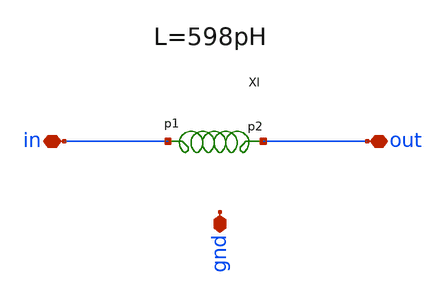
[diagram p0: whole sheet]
** sch_path: impedance-transformer/xschem/impedance-transformer-pex.sch
**.subckt impedance-transformer-pex gnd in out
*.iopin gnd
*.iopin in
*.iopin out
xl1 in out l1
**** begin user architecture code

* NGSPICE file created from impedance-transformer.ext - technology: sky130A

.subckt sky130_fd_pr__cap_mim_m3_2_4GE4YE c2_n2372_n7179# m4_n2472_n7279# VSUBS
X0 c2_n2372_n7179# m4_n2472_n7279# sky130_fd_pr__cap_mim_m3_2 l=2.293e+07u w=2.293e+07u
X1 c2_n2372_n7179# m4_n2472_n7279# sky130_fd_pr__cap_mim_m3_2 l=2.293e+07u w=2.293e+07u
X2 c2_n2372_n7179# m4_n2472_n7279# sky130_fd_pr__cap_mim_m3_2 l=2.293e+07u w=2.293e+07u
C0 m4_n2472_n7279# c2_n2372_n7179# 105.86fF
C1 c2_n2372_n7179# VSUBS 0.26fF
C2 m4_n2472_n7279# VSUBS 28.10fF
.ends

.subckt sky130_fd_pr__cap_mim_m3_2_8BWDGQ c2_n2486_n10078# m4_n2586_n10178# VSUBS
X0 c2_n2486_n10078# m4_n2586_n10178# sky130_fd_pr__cap_mim_m3_2 l=2.407e+07u w=2.407e+07u
X1 c2_n2486_n10078# m4_n2586_n10178# sky130_fd_pr__cap_mim_m3_2 l=2.407e+07u w=2.407e+07u
X2 c2_n2486_n10078# m4_n2586_n10178# sky130_fd_pr__cap_mim_m3_2 l=2.407e+07u w=2.407e+07u
X3 c2_n2486_n10078# m4_n2586_n10178# sky130_fd_pr__cap_mim_m3_2 l=2.407e+07u w=2.407e+07u
C0 m4_n2586_n10178# c2_n2486_n10078# 154.16fF
C1 c2_n2486_n10078# VSUBS 0.30fF
C2 m4_n2586_n10178# VSUBS 40.10fF
.ends

*.subckt impedance-transformer gnd out in
Xsky130_fd_pr__cap_mim_m3_2_4GE4YE_1 in gnd gnd sky130_fd_pr__cap_mim_m3_2_4GE4YE
Xsky130_fd_pr__cap_mim_m3_2_4GE4YE_2 in gnd gnd sky130_fd_pr__cap_mim_m3_2_4GE4YE
Xsky130_fd_pr__cap_mim_m3_2_8BWDGQ_0 out gnd gnd sky130_fd_pr__cap_mim_m3_2_8BWDGQ
Xsky130_fd_pr__cap_mim_m3_2_8BWDGQ_1 out gnd gnd sky130_fd_pr__cap_mim_m3_2_8BWDGQ
Xsky130_fd_pr__cap_mim_m3_2_8BWDGQ_2 out gnd gnd sky130_fd_pr__cap_mim_m3_2_8BWDGQ
Xsky130_fd_pr__cap_mim_m3_2_8BWDGQ_3 out gnd gnd sky130_fd_pr__cap_mim_m3_2_8BWDGQ
Xsky130_fd_pr__cap_mim_m3_2_4GE4YE_0 in gnd gnd sky130_fd_pr__cap_mim_m3_2_4GE4YE

R0 in in.n1 0.704
R1 in.n0 in.t3 0.125
R2 in.n1 in.n0 0.089
R3 in.t8 in.t7 0.066
R4 in.t6 in.t8 0.066
R5 in.t2 in.t1 0.066
R6 in.t0 in.t2 0.066
R7 in.t5 in.t4 0.066
R8 in.t3 in.t5 0.066
R9 in.n1 in.t6 0.037
R10 in.n0 in.t0 0.037
R11 out out.n2 0.325
R12 out.n0 out.t13 0.094
R13 out.n1 out.n0 0.079
R14 out.t14 out.t15 0.066
R15 out.t12 out.t14 0.066
R16 out.t13 out.t12 0.066
R17 out.t10 out.t11 0.066
R18 out.t8 out.t10 0.066
R19 out.t9 out.t8 0.066
R20 out.t6 out.t7 0.066
R21 out.t4 out.t6 0.066
R22 out.t5 out.t4 0.066
R23 out.t2 out.t3 0.066
R24 out.t0 out.t2 0.066
R25 out.t1 out.t0 0.066
R26 out.n2 out.n1 0.064
R27 out.n2 out.t1 0.041
R28 out.n0 out.t9 0.018
R29 out.n1 out.t5 0.018
C0 out.t7 gnd 33.56fF
C1 out.t6 gnd 33.64fF
C2 out.t4 gnd 33.64fF
C3 out.t5 gnd 29.89fF
C4 out.t11 gnd 33.56fF
C5 out.t10 gnd 33.64fF
C6 out.t8 gnd 33.64fF
C7 out.t9 gnd 29.89fF
C8 out.t15 gnd 33.56fF
C9 out.t14 gnd 33.64fF
C10 out.t12 gnd 33.64fF
C11 out.t13 gnd 89.97fF
C12 out.n0 gnd 28.18fF $ **FLOATING
C13 out.n1 gnd 13.26fF $ **FLOATING
C14 out.t3 gnd 33.56fF
C15 out.t2 gnd 33.64fF
C16 out.t0 gnd 33.64fF
C17 out.t1 gnd 33.03fF
C18 out.n2 gnd 41.48fF $ **FLOATING
C19 in.t7 gnd 32.16fF
C20 in.t8 gnd 32.25fF
C21 in.t6 gnd 30.87fF
C22 in.t1 gnd 32.16fF
C23 in.t2 gnd 32.25fF
C24 in.t0 gnd 30.87fF
C25 in.t4 gnd 32.16fF
C26 in.t5 gnd 32.25fF
C27 in.t3 gnd 30.02fF
C28 in.n0 gnd 11.26fF $ **FLOATING
C29 in.n1 gnd 57.09fF $ **FLOATING
C30 in gnd 55.98fF
C31 out gnd 70.58fF
*.ends



**** end user architecture code
**.ends

* expanding   symbol:  /home/hugodg/projects_sky130/temp_sensor/impedance-transformer/xschem/l1.sym
*+ # of pins=2
** sym_path: impedance-transformer/xschem/l1.sym
** sch_path: impedance-transformer/xschem/l1.sch
.subckt l1 p1 p2
*.iopin p2
*.iopin p1
L0 p1 net3 598p m=1
Cs1 p1 net1 26.59f m=1
Cs2 p2 net2 25.14f m=1
Rs1 net1 GND 63.55 m=1
Rs2 net2 GND 19.11 m=1
R1 p2 net3 2.89 m=1
.ends

.GLOBAL GND
.end
